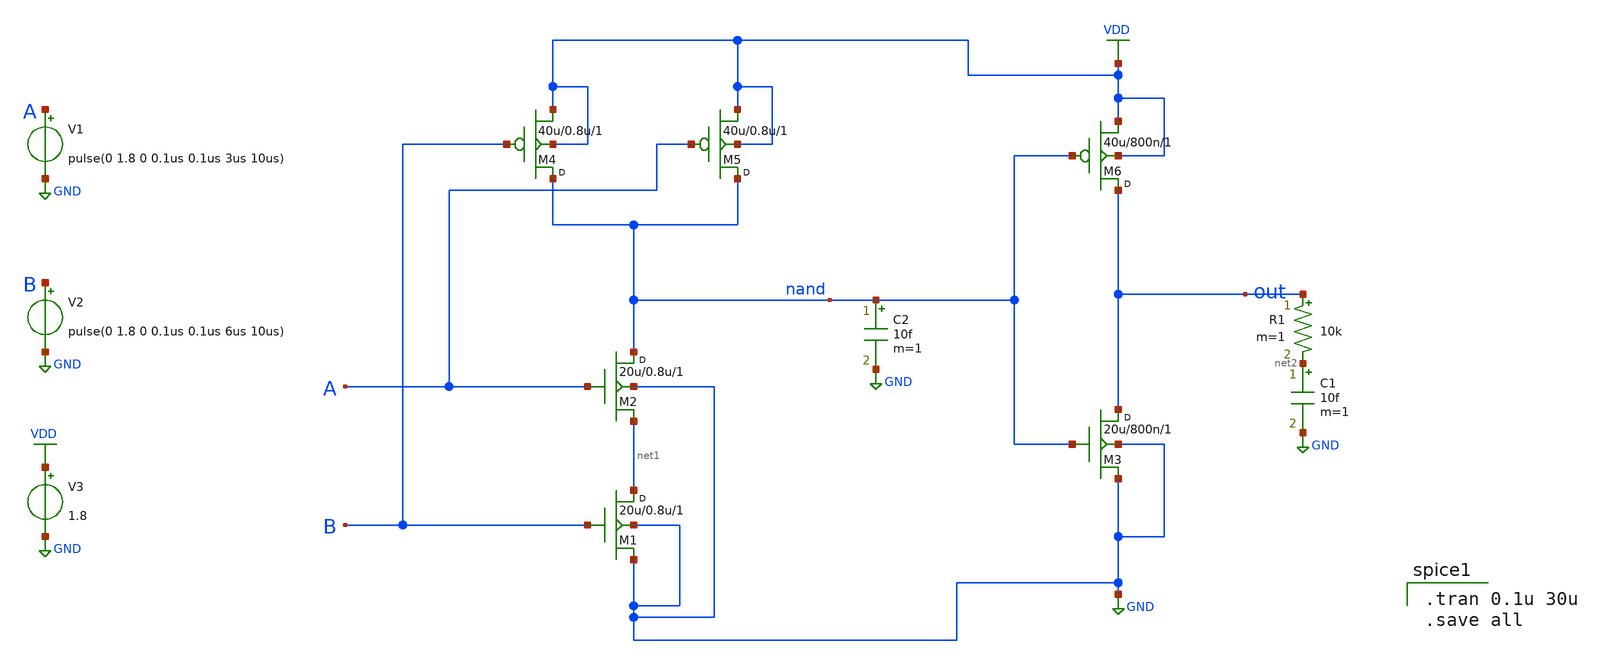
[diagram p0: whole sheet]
** sch_path: cells/and2/AND.sch
**.subckt AND
M1 net1 B GND GND nmos w=20u l=0.8u m=1
M2 nand A net1 GND nmos w=20u l=0.8u m=1
M3 out nand GND GND nmos w=20u l=800n m=1
M4 nand B VDD VDD pmos w=40u l=0.8u m=1
M5 nand A VDD VDD pmos w=40u l=0.8u m=1
M6 out nand VDD VDD pmos w=40u l=800n m=1
V1 A GND pulse(0 1.8 0 0.1us 0.1us 3us 10us)
V2 B GND pulse(0 1.8 0 0.1us 0.1us 6us 10us)
V3 VDD GND 1.8
R1 out net2 10k m=1
C1 net2 GND 10f m=1
C2 nand GND 10f m=1
**** begin user architecture code



.model pmos pmos level=49 version=3.3.0


.tran 0.1u 30u
.save all

**** end user architecture code
**.ends
.GLOBAL GND
.GLOBAL VDD
**** begin user architecture code


.model nmos nmos level=49 version=3.3.0


**** end user architecture code
.end
